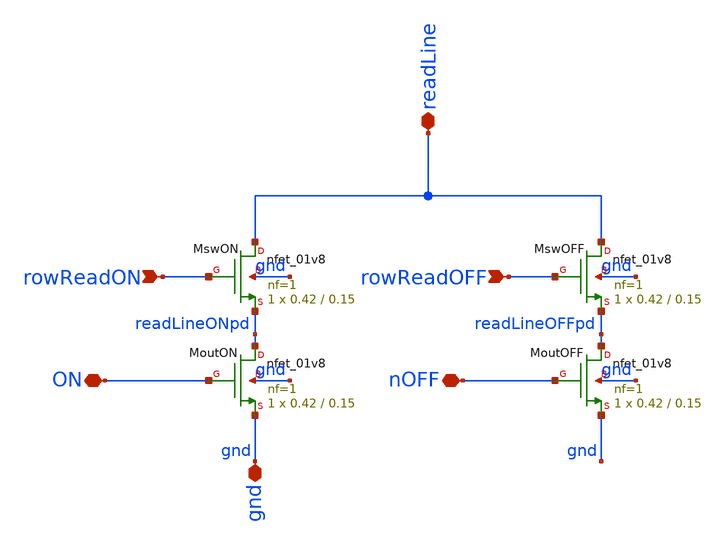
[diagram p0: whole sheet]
** sch_path: analog/xschem/PixelHandshake.sch
**.subckt PixelHandshake rowReadON rowReadOFF readLine ON nOFF gnd
*.ipin rowReadON
*.ipin rowReadOFF
*.iopin readLine
*.iopin ON
*.iopin nOFF
*.iopin gnd
XMswON readLine rowReadON readLineONpd gnd sky130_fd_pr__nfet_01v8 L=0.15 W=0.42 nf=1 ad='int((1 + 1)/2) * 0.42 / 1 * 0.29'
+ as='int((1 + 2)/2) * 0.42 / 1 * 0.29' pd='2*int((1 + 1)/2) * (0.42 / 1 + 0.29)' ps='2*int((1 + 2)/2) * (0.42 / 1 + 0.29)'
+ nrd='0.29 / 0.42 ' nrs='0.29 / 0.42 ' sa=0 sb=0 sd=0 mult=1 m=1
XMoutON readLineONpd ON gnd gnd sky130_fd_pr__nfet_01v8 L=0.15 W=0.42 nf=1 ad='int((1 + 1)/2) * 0.42 / 1 * 0.29'
+ as='int((1 + 2)/2) * 0.42 / 1 * 0.29' pd='2*int((1 + 1)/2) * (0.42 / 1 + 0.29)' ps='2*int((1 + 2)/2) * (0.42 / 1 + 0.29)'
+ nrd='0.29 / 0.42 ' nrs='0.29 / 0.42 ' sa=0 sb=0 sd=0 mult=1 m=1
XMswOFF readLine rowReadOFF readLineOFFpd gnd sky130_fd_pr__nfet_01v8 L=0.15 W=0.42 nf=1 ad='int((1 + 1)/2) * 0.42 / 1 * 0.29'
+ as='int((1 + 2)/2) * 0.42 / 1 * 0.29' pd='2*int((1 + 1)/2) * (0.42 / 1 + 0.29)' ps='2*int((1 + 2)/2) * (0.42 / 1 + 0.29)'
+ nrd='0.29 / 0.42 ' nrs='0.29 / 0.42 ' sa=0 sb=0 sd=0 mult=1 m=1
XMoutOFF readLineOFFpd nOFF gnd gnd sky130_fd_pr__nfet_01v8 L=0.15 W=0.42 nf=1 ad='int((1 + 1)/2) * 0.42 / 1 * 0.29'
+ as='int((1 + 2)/2) * 0.42 / 1 * 0.29' pd='2*int((1 + 1)/2) * (0.42 / 1 + 0.29)' ps='2*int((1 + 2)/2) * (0.42 / 1 + 0.29)'
+ nrd='0.29 / 0.42 ' nrs='0.29 / 0.42 ' sa=0 sb=0 sd=0 mult=1 m=1
**.ends
.end
